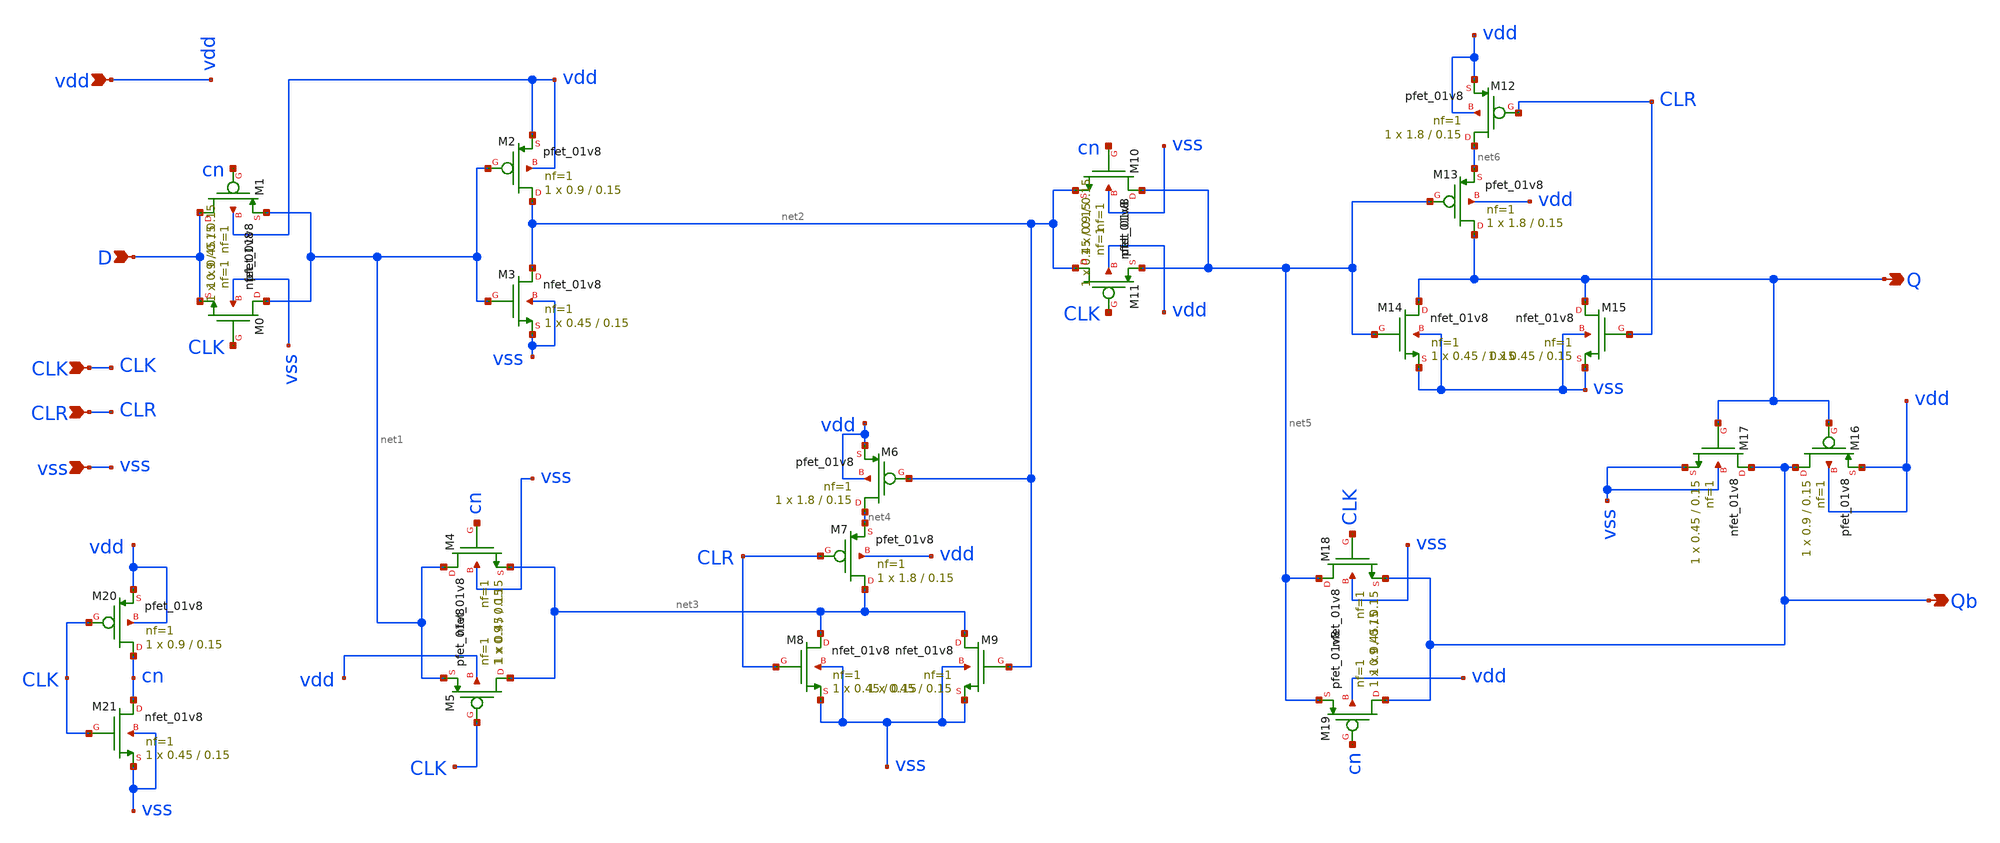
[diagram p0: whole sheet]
** sch_path: track_vlsi/ledesma/sch/ffdc.sch
**.subckt ffdc D vdd Q Qb CLK CLR vss
*.ipin D
*.ipin vdd
*.opin Q
*.opin Qb
*.ipin CLK
*.ipin CLR
*.ipin vss
XM0 net1 CLK D vss sky130_fd_pr__nfet_01v8 L=0.15 W=0.45 nf=1 ad='int((nf+1)/2) * W/nf * 0.29' as='int((nf+2)/2) * W/nf * 0.29'
+ pd='2*int((nf+1)/2) * (W/nf + 0.29)' ps='2*int((nf+2)/2) * (W/nf + 0.29)' nrd='0.29 / W' nrs='0.29 / W'
+ sa=0 sb=0 sd=0 mult=1 m=1
XM1 D cn net1 vdd sky130_fd_pr__pfet_01v8 L=0.15 W=0.9 nf=1 ad='int((nf+1)/2) * W/nf * 0.29' as='int((nf+2)/2) * W/nf * 0.29'
+ pd='2*int((nf+1)/2) * (W/nf + 0.29)' ps='2*int((nf+2)/2) * (W/nf + 0.29)' nrd='0.29 / W' nrs='0.29 / W'
+ sa=0 sb=0 sd=0 mult=1 m=1
XM2 net2 net1 vdd vdd sky130_fd_pr__pfet_01v8 L=0.15 W=0.9 nf=1 ad='int((nf+1)/2) * W/nf * 0.29' as='int((nf+2)/2) * W/nf * 0.29'
+ pd='2*int((nf+1)/2) * (W/nf + 0.29)' ps='2*int((nf+2)/2) * (W/nf + 0.29)' nrd='0.29 / W' nrs='0.29 / W'
+ sa=0 sb=0 sd=0 mult=1 m=1
XM3 net2 net1 vss vss sky130_fd_pr__nfet_01v8 L=0.15 W=0.45 nf=1 ad='int((nf+1)/2) * W/nf * 0.29' as='int((nf+2)/2) * W/nf * 0.29'
+ pd='2*int((nf+1)/2) * (W/nf + 0.29)' ps='2*int((nf+2)/2) * (W/nf + 0.29)' nrd='0.29 / W' nrs='0.29 / W'
+ sa=0 sb=0 sd=0 mult=1 m=1
XM4 net1 cn net3 vss sky130_fd_pr__nfet_01v8 L=0.15 W=0.45 nf=1 ad='int((nf+1)/2) * W/nf * 0.29' as='int((nf+2)/2) * W/nf * 0.29'
+ pd='2*int((nf+1)/2) * (W/nf + 0.29)' ps='2*int((nf+2)/2) * (W/nf + 0.29)' nrd='0.29 / W' nrs='0.29 / W'
+ sa=0 sb=0 sd=0 mult=1 m=1
XM5 net3 CLK net1 vdd sky130_fd_pr__pfet_01v8 L=0.15 W=0.9 nf=1 ad='int((nf+1)/2) * W/nf * 0.29' as='int((nf+2)/2) * W/nf * 0.29'
+ pd='2*int((nf+1)/2) * (W/nf + 0.29)' ps='2*int((nf+2)/2) * (W/nf + 0.29)' nrd='0.29 / W' nrs='0.29 / W'
+ sa=0 sb=0 sd=0 mult=1 m=1
XM6 net4 net2 vdd vdd sky130_fd_pr__pfet_01v8 L=0.15 W=1.8 nf=1 ad='int((nf+1)/2) * W/nf * 0.29' as='int((nf+2)/2) * W/nf * 0.29'
+ pd='2*int((nf+1)/2) * (W/nf + 0.29)' ps='2*int((nf+2)/2) * (W/nf + 0.29)' nrd='0.29 / W' nrs='0.29 / W'
+ sa=0 sb=0 sd=0 mult=1 m=1
XM7 net3 CLR net4 vdd sky130_fd_pr__pfet_01v8 L=0.15 W=1.8 nf=1 ad='int((nf+1)/2) * W/nf * 0.29' as='int((nf+2)/2) * W/nf * 0.29'
+ pd='2*int((nf+1)/2) * (W/nf + 0.29)' ps='2*int((nf+2)/2) * (W/nf + 0.29)' nrd='0.29 / W' nrs='0.29 / W'
+ sa=0 sb=0 sd=0 mult=1 m=1
XM8 net3 CLR vss vss sky130_fd_pr__nfet_01v8 L=0.15 W=0.45 nf=1 ad='int((nf+1)/2) * W/nf * 0.29' as='int((nf+2)/2) * W/nf * 0.29'
+ pd='2*int((nf+1)/2) * (W/nf + 0.29)' ps='2*int((nf+2)/2) * (W/nf + 0.29)' nrd='0.29 / W' nrs='0.29 / W'
+ sa=0 sb=0 sd=0 mult=1 m=1
XM9 net3 net2 vss vss sky130_fd_pr__nfet_01v8 L=0.15 W=0.45 nf=1 ad='int((nf+1)/2) * W/nf * 0.29' as='int((nf+2)/2) * W/nf * 0.29'
+ pd='2*int((nf+1)/2) * (W/nf + 0.29)' ps='2*int((nf+2)/2) * (W/nf + 0.29)' nrd='0.29 / W' nrs='0.29 / W'
+ sa=0 sb=0 sd=0 mult=1 m=1
XM10 net5 cn net2 vss sky130_fd_pr__nfet_01v8 L=0.15 W=0.45 nf=1 ad='int((nf+1)/2) * W/nf * 0.29' as='int((nf+2)/2) * W/nf * 0.29'
+ pd='2*int((nf+1)/2) * (W/nf + 0.29)' ps='2*int((nf+2)/2) * (W/nf + 0.29)' nrd='0.29 / W' nrs='0.29 / W'
+ sa=0 sb=0 sd=0 mult=1 m=1
XM11 net2 CLK net5 vdd sky130_fd_pr__pfet_01v8 L=0.15 W=0.9 nf=1 ad='int((nf+1)/2) * W/nf * 0.29' as='int((nf+2)/2) * W/nf * 0.29'
+ pd='2*int((nf+1)/2) * (W/nf + 0.29)' ps='2*int((nf+2)/2) * (W/nf + 0.29)' nrd='0.29 / W' nrs='0.29 / W'
+ sa=0 sb=0 sd=0 mult=1 m=1
XM12 net6 CLR vdd vdd sky130_fd_pr__pfet_01v8 L=0.15 W=1.8 nf=1 ad='int((nf+1)/2) * W/nf * 0.29' as='int((nf+2)/2) * W/nf * 0.29'
+ pd='2*int((nf+1)/2) * (W/nf + 0.29)' ps='2*int((nf+2)/2) * (W/nf + 0.29)' nrd='0.29 / W' nrs='0.29 / W'
+ sa=0 sb=0 sd=0 mult=1 m=1
XM13 Q net5 net6 vdd sky130_fd_pr__pfet_01v8 L=0.15 W=1.8 nf=1 ad='int((nf+1)/2) * W/nf * 0.29' as='int((nf+2)/2) * W/nf * 0.29'
+ pd='2*int((nf+1)/2) * (W/nf + 0.29)' ps='2*int((nf+2)/2) * (W/nf + 0.29)' nrd='0.29 / W' nrs='0.29 / W'
+ sa=0 sb=0 sd=0 mult=1 m=1
XM14 Q net5 vss vss sky130_fd_pr__nfet_01v8 L=0.15 W=0.45 nf=1 ad='int((nf+1)/2) * W/nf * 0.29' as='int((nf+2)/2) * W/nf * 0.29'
+ pd='2*int((nf+1)/2) * (W/nf + 0.29)' ps='2*int((nf+2)/2) * (W/nf + 0.29)' nrd='0.29 / W' nrs='0.29 / W'
+ sa=0 sb=0 sd=0 mult=1 m=1
XM15 Q CLR vss vss sky130_fd_pr__nfet_01v8 L=0.15 W=0.45 nf=1 ad='int((nf+1)/2) * W/nf * 0.29' as='int((nf+2)/2) * W/nf * 0.29'
+ pd='2*int((nf+1)/2) * (W/nf + 0.29)' ps='2*int((nf+2)/2) * (W/nf + 0.29)' nrd='0.29 / W' nrs='0.29 / W'
+ sa=0 sb=0 sd=0 mult=1 m=1
XM16 Qb Q vdd vdd sky130_fd_pr__pfet_01v8 L=0.15 W=0.9 nf=1 ad='int((nf+1)/2) * W/nf * 0.29' as='int((nf+2)/2) * W/nf * 0.29'
+ pd='2*int((nf+1)/2) * (W/nf + 0.29)' ps='2*int((nf+2)/2) * (W/nf + 0.29)' nrd='0.29 / W' nrs='0.29 / W'
+ sa=0 sb=0 sd=0 mult=1 m=1
XM17 Qb Q vss vss sky130_fd_pr__nfet_01v8 L=0.15 W=0.45 nf=1 ad='int((nf+1)/2) * W/nf * 0.29' as='int((nf+2)/2) * W/nf * 0.29'
+ pd='2*int((nf+1)/2) * (W/nf + 0.29)' ps='2*int((nf+2)/2) * (W/nf + 0.29)' nrd='0.29 / W' nrs='0.29 / W'
+ sa=0 sb=0 sd=0 mult=1 m=1
XM18 net5 CLK Qb vss sky130_fd_pr__nfet_01v8 L=0.15 W=0.45 nf=1 ad='int((nf+1)/2) * W/nf * 0.29' as='int((nf+2)/2) * W/nf * 0.29'
+ pd='2*int((nf+1)/2) * (W/nf + 0.29)' ps='2*int((nf+2)/2) * (W/nf + 0.29)' nrd='0.29 / W' nrs='0.29 / W'
+ sa=0 sb=0 sd=0 mult=1 m=1
XM19 Qb cn net5 vdd sky130_fd_pr__pfet_01v8 L=0.15 W=0.9 nf=1 ad='int((nf+1)/2) * W/nf * 0.29' as='int((nf+2)/2) * W/nf * 0.29'
+ pd='2*int((nf+1)/2) * (W/nf + 0.29)' ps='2*int((nf+2)/2) * (W/nf + 0.29)' nrd='0.29 / W' nrs='0.29 / W'
+ sa=0 sb=0 sd=0 mult=1 m=1
XM20 cn CLK vdd vdd sky130_fd_pr__pfet_01v8 L=0.15 W=0.9 nf=1 ad='int((nf+1)/2) * W/nf * 0.29' as='int((nf+2)/2) * W/nf * 0.29'
+ pd='2*int((nf+1)/2) * (W/nf + 0.29)' ps='2*int((nf+2)/2) * (W/nf + 0.29)' nrd='0.29 / W' nrs='0.29 / W'
+ sa=0 sb=0 sd=0 mult=1 m=1
XM21 cn CLK vss vss sky130_fd_pr__nfet_01v8 L=0.15 W=0.45 nf=1 ad='int((nf+1)/2) * W/nf * 0.29' as='int((nf+2)/2) * W/nf * 0.29'
+ pd='2*int((nf+1)/2) * (W/nf + 0.29)' ps='2*int((nf+2)/2) * (W/nf + 0.29)' nrd='0.29 / W' nrs='0.29 / W'
+ sa=0 sb=0 sd=0 mult=1 m=1
**.ends
.end
